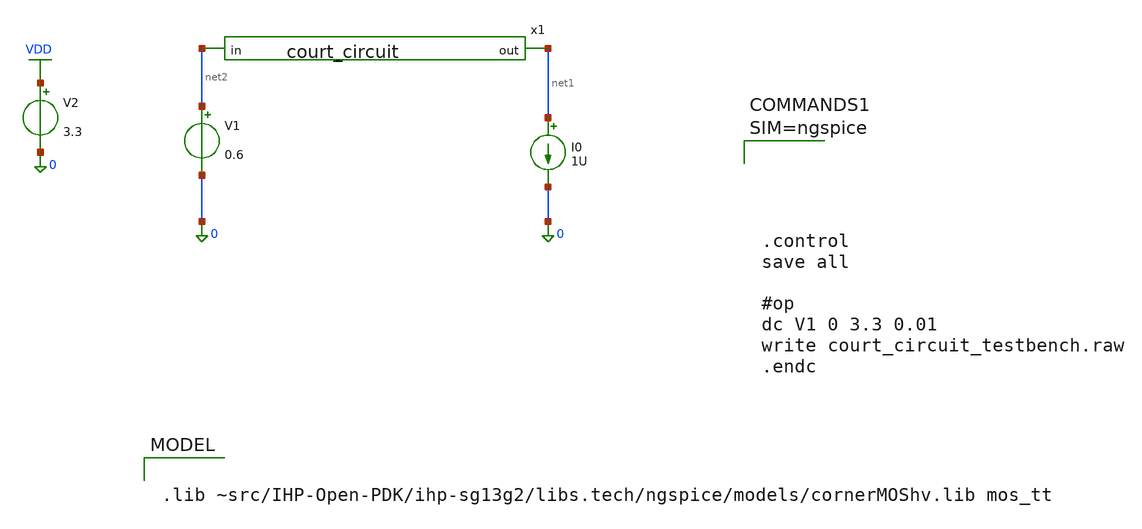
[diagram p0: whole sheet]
** sch_path: court_circuit_actif/court_circuit_testbench.sch
**.subckt court_circuit_testbench
x1 net1 net2 court_circuit
V1 net2 0 0.6
I0 net1 0 1U
V2 VDD 0 3.3
**** begin user architecture code






.control
save all

#op
dc V1 0 3.3 0.01
write court_circuit_testbench.raw
.endc




.lib ~src/IHP-Open-PDK/ihp-sg13g2/libs.tech/ngspice/models/cornerMOShv.lib mos_tt
**** end user architecture code
**.ends
.GLOBAL VDD
.end
